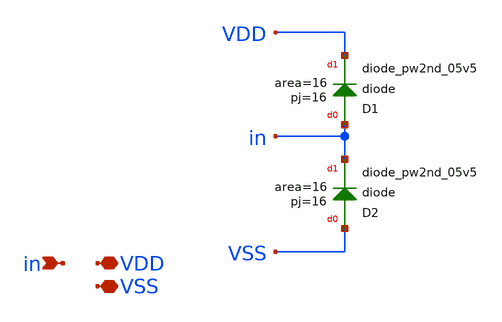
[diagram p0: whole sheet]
** sch_path: xschem/src/esd_diodes/esd_diodes.sch
**.subckt esd_diodes VDD in VSS
*.iopin VDD
*.ipin in
*.iopin VSS
XD1 in VDD sky130_fd_pr__diode_pw2nd_05v5 area=16 pj=16
XD2 VSS in sky130_fd_pr__diode_pw2nd_05v5 area=16 pj=16
**.ends
.end
